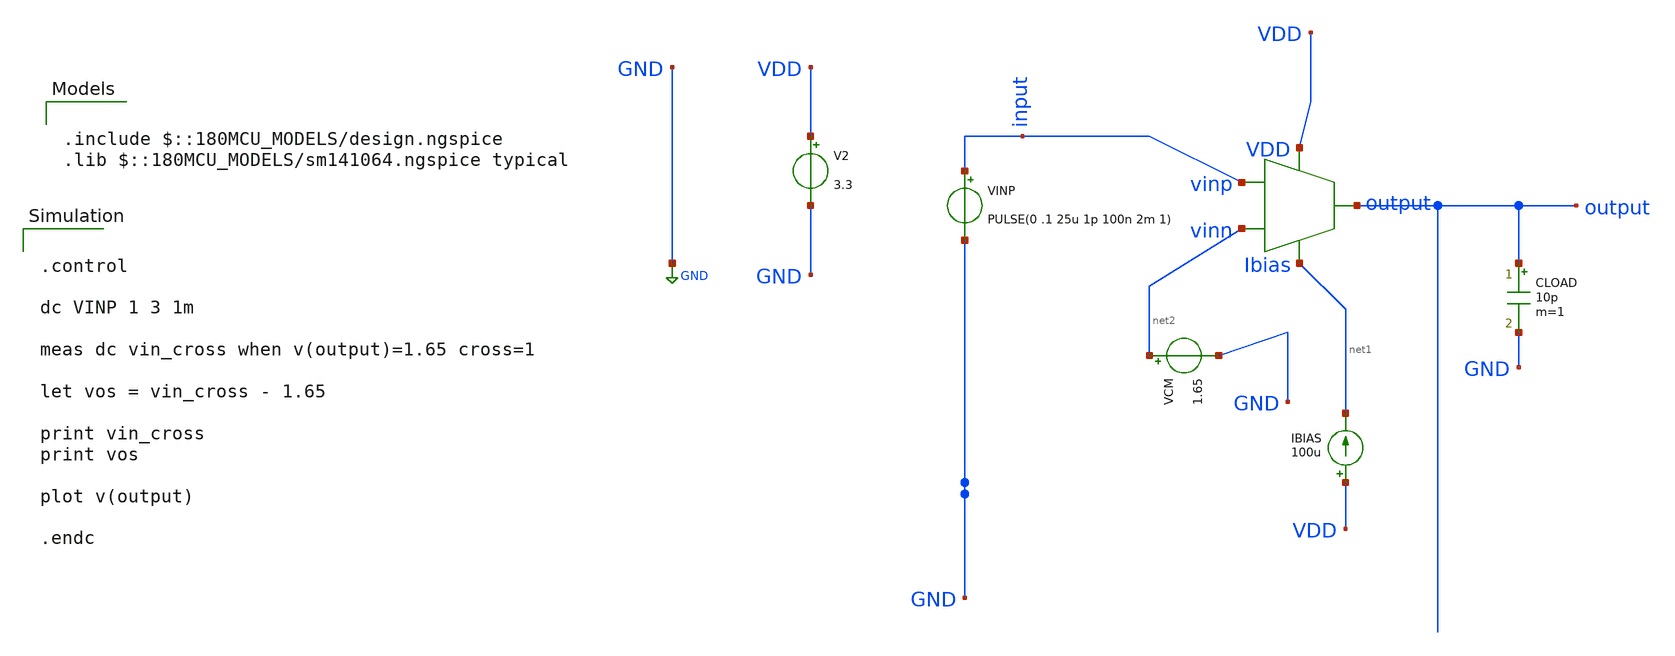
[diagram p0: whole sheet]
** sch_path: designs/libs/core_amps/ota_telescopic/telescopic_vos_tb.sch
**.subckt telescopic_vos_tb
IBIAS VDD net1 100u
V2 VDD GND 3.3
CLOAD output GND 10p m=1
VINP input GND PULSE(0 .1 25u 1p 100n 2m 1)
VCM net2 GND 1.65
X1 input net2 VDD net1 output telescopic_cascode
**** begin user architecture code

.include $::180MCU_MODELS/design.ngspice
.lib $::180MCU_MODELS/sm141064.ngspice typical



.control

dc VINP 1 3 1m

meas dc vin_cross when v(output)=1.65 cross=1

let vos = vin_cross - 1.65

print vin_cross
print vos

plot v(output)

.endc


**** end user architecture code
**.ends

* expanding   symbol:  libs/core_amps/ota_telescopic/telescopic_cascode.sym # of pins=5
** sym_path: designs/libs/core_amps/ota_telescopic/telescopic_cascode.sym
** sch_path: designs/libs/core_amps/ota_telescopic/telescopic_cascode.sch
.subckt telescopic_cascode vinp vinn VDD Ibias output
*.ipin vinp
*.ipin vinn
*.opin output
*.iopin Ibias
*.iopin VDD
XM8 output net4 net3 VDD pfet_03v3 L=0.56u W=65u nf=1 ad='int((nf+1)/2) * W/nf * 0.18u' as='int((nf+2)/2) * W/nf * 0.18u'
+ pd='2*int((nf+1)/2) * (W/nf + 0.18u)' ps='2*int((nf+2)/2) * (W/nf + 0.18u)' nrd='0.18u / W' nrs='0.18u / W'
+ sa=0 sb=0 sd=0 m=4
XM4 output VBN1 net7 GND nfet_03v3 L=0.5u W=40u nf=1 ad='int((nf+1)/2) * W/nf * 0.18u' as='int((nf+2)/2) * W/nf * 0.18u'
+ pd='2*int((nf+1)/2) * (W/nf + 0.18u)' ps='2*int((nf+2)/2) * (W/nf + 0.18u)' nrd='0.18u / W' nrs='0.18u / W'
+ sa=0 sb=0 sd=0 m=1
XM1 net5 vinp net6 GND nfet_03v3 L=0.5u W=30u nf=1 ad='int((nf+1)/2) * W/nf * 0.18u' as='int((nf+2)/2) * W/nf * 0.18u'
+ pd='2*int((nf+1)/2) * (W/nf + 0.18u)' ps='2*int((nf+2)/2) * (W/nf + 0.18u)' nrd='0.18u / W' nrs='0.18u / W'
+ sa=0 sb=0 sd=0 m=1
XM2 net1 VBN1 net5 GND nfet_03v3 L=0.5u W=40u nf=1 ad='int((nf+1)/2) * W/nf * 0.18u' as='int((nf+2)/2) * W/nf * 0.18u'
+ pd='2*int((nf+1)/2) * (W/nf + 0.18u)' ps='2*int((nf+2)/2) * (W/nf + 0.18u)' nrd='0.18u / W' nrs='0.18u / W'
+ sa=0 sb=0 sd=0 m=1
XM3 net7 vinn net6 GND nfet_03v3 L=0.5u W=30u nf=1 ad='int((nf+1)/2) * W/nf * 0.18u' as='int((nf+2)/2) * W/nf * 0.18u'
+ pd='2*int((nf+1)/2) * (W/nf + 0.18u)' ps='2*int((nf+2)/2) * (W/nf + 0.18u)' nrd='0.18u / W' nrs='0.18u / W'
+ sa=0 sb=0 sd=0 m=1
XM5 net3 net1 VDD VDD pfet_03v3 L=0.56u W=65u nf=1 ad='int((nf+1)/2) * W/nf * 0.18u' as='int((nf+2)/2) * W/nf * 0.18u'
+ pd='2*int((nf+1)/2) * (W/nf + 0.18u)' ps='2*int((nf+2)/2) * (W/nf + 0.18u)' nrd='0.18u / W' nrs='0.18u / W'
+ sa=0 sb=0 sd=0 m=4
XM6 net1 net4 net2 VDD pfet_03v3 L=0.56u W=65u nf=1 ad='int((nf+1)/2) * W/nf * 0.18u' as='int((nf+2)/2) * W/nf * 0.18u'
+ pd='2*int((nf+1)/2) * (W/nf + 0.18u)' ps='2*int((nf+2)/2) * (W/nf + 0.18u)' nrd='0.18u / W' nrs='0.18u / W'
+ sa=0 sb=0 sd=0 m=4
XM7 net2 net1 VDD VDD pfet_03v3 L=0.56u W=65u nf=1 ad='int((nf+1)/2) * W/nf * 0.18u' as='int((nf+2)/2) * W/nf * 0.18u'
+ pd='2*int((nf+1)/2) * (W/nf + 0.18u)' ps='2*int((nf+2)/2) * (W/nf + 0.18u)' nrd='0.18u / W' nrs='0.18u / W'
+ sa=0 sb=0 sd=0 m=4
XM9 net6 Ibias GND GND nfet_03v3 L=0.28u W=15.54u nf=1 ad='int((nf+1)/2) * W/nf * 0.18u' as='int((nf+2)/2) * W/nf * 0.18u'
+ pd='2*int((nf+1)/2) * (W/nf + 0.18u)' ps='2*int((nf+2)/2) * (W/nf + 0.18u)' nrd='0.18u / W' nrs='0.18u / W'
+ sa=0 sb=0 sd=0 m=1
XM10 Ibias Ibias GND GND nfet_03v3 L=.28u W=5.18u nf=1 ad='int((nf+1)/2) * W/nf * 0.18u' as='int((nf+2)/2) * W/nf * 0.18u'
+ pd='2*int((nf+1)/2) * (W/nf + 0.18u)' ps='2*int((nf+2)/2) * (W/nf + 0.18u)' nrd='0.18u / W' nrs='0.18u / W'
+ sa=0 sb=0 sd=0 m=1
**** begin user architecture code


.include /foss/pdks/gf180mcuD/libs.tech/ngspice/design.ngspice
.lib /foss/pdks/gf180mcuD/libs.tech/ngspice/sm141064.ngspice typical

**** end user architecture code
V1 VBN1 GND 2.2
V2 net4 GND 1.6
.ends

.GLOBAL GND
.end
